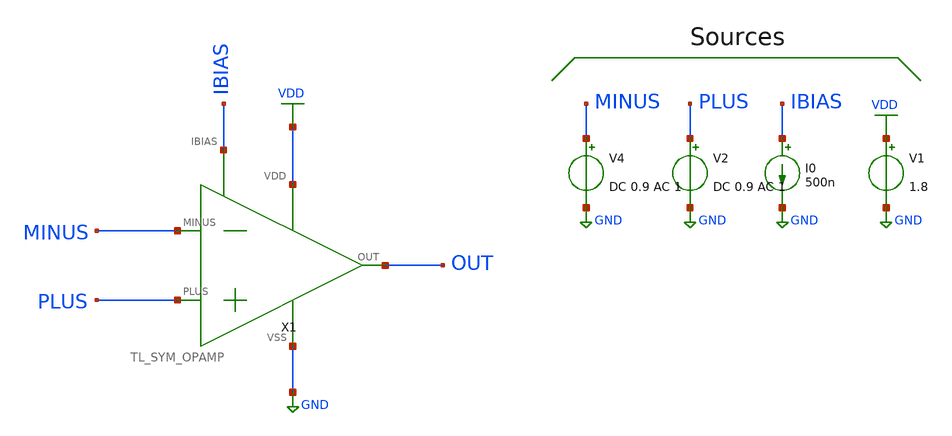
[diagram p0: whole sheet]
** sch_path: xschem/MISC/TL_OPAMP.sch
**.subckt TL_OPAMP
I0 IBIAS GND 500n
V1 VDD GND 1.8
V2 PLUS GND DC 0.9 AC 1
V4 MINUS GND DC 0.9 AC 1
X1 PLUS MINUS OUT IBIAS GND VDD TL_SYM_OPAMP
**** begin user architecture code



*.include ~/OpenPDK/skywater-pdk/skywater-pdk/libraries/sky130_fd_pr/latest/cells/pfet_g5v0d10v5/sky130_fd_pr__pfet_g5v0d10v5__tt.corner.spice
*.include ~/OpenPDK/skywater-pdk/skywater-pdk/libraries/sky130_fd_pr/latest/cells/pfet_g5v0d10v5/sky130_fd_pr__pfet_g5v0d10v5__mismatch.corner.spice
*.include ~/OpenPDK/skywater-pdk/skywater-pdk/libraries/sky130_fd_pr/latest/cells/pfet_g5v0d10v5/sky130_fd_pr__nfet_g5v0d10v5__tt.corner.spice
*.include ~/OpenPDK/skywater-pdk/skywater-pdk/libraries/sky130_fd_pr/latest/cells/pfet_g5v0d10v5/sky130_fd_pr__nfet_g5v0d10v5__mismatch.corner.spice

.include /usr/share/pdk/sky130A/libs.ref/spi/sky130_fd_pr/sky130_fd_pr__nfet_01v8_lvt__tt.corner.spice
.include /usr/share/pdk/sky130A/libs.ref/spi/sky130_fd_pr/sky130_fd_pr__nfet_01v8_lvt__mismatch.corner.spice
.include /usr/share/pdk/sky130A/libs.ref/spi/sky130_fd_pr/sky130_fd_pr__pfet_01v8_lvt__tt.corner.spice
.include /usr/share/pdk/sky130A/libs.ref/spi/sky130_fd_pr/sky130_fd_pr__pfet_01v8_lvt__mismatch.corner.spice

.include ~/OpenPDK/skywater-pdk/skywater-pdk/libraries/sky130_fd_pr/latest/models/all.spice





.control

op
dc V2 0.85 0.95 100u
plot OUT
plot deriv(OUT)

.endc


**** end user architecture code
**.ends
.GLOBAL VDD
.GLOBAL GND
.end
